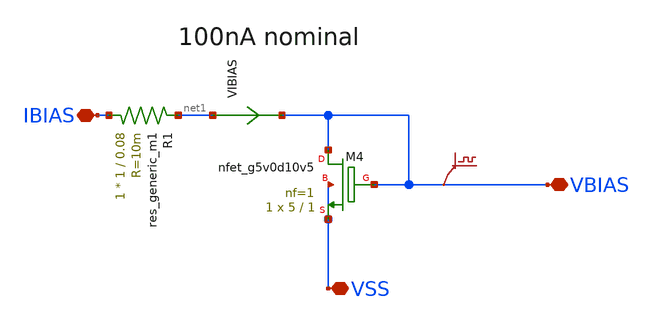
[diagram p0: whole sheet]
** sch_path: xschem/vbias_gen_pga.sch
**.subckt vbias_gen_pga VBIAS VSS IBIAS
*.iopin VBIAS
*.iopin VSS
*.iopin IBIAS
.save v(vbias)
VIBIAS net1 VBIAS 0
.save i(vibias)
XM4 VBIAS VBIAS VSS VSS sky130_fd_pr__nfet_g5v0d10v5 L=1 W=5 nf=1 ad='int((nf+1)/2) * W/nf * 0.29' as='int((nf+2)/2) * W/nf * 0.29'
+ pd='2*int((nf+1)/2) * (W/nf + 0.29)' ps='2*int((nf+2)/2) * (W/nf + 0.29)' nrd='0.29 / W' nrs='0.29 / W'
+ sa=0 sb=0 sd=0 mult=1 m=1
R1 IBIAS net1 sky130_fd_pr__res_generic_m1 W=1 L=0.08 m=1
**.ends
.end
